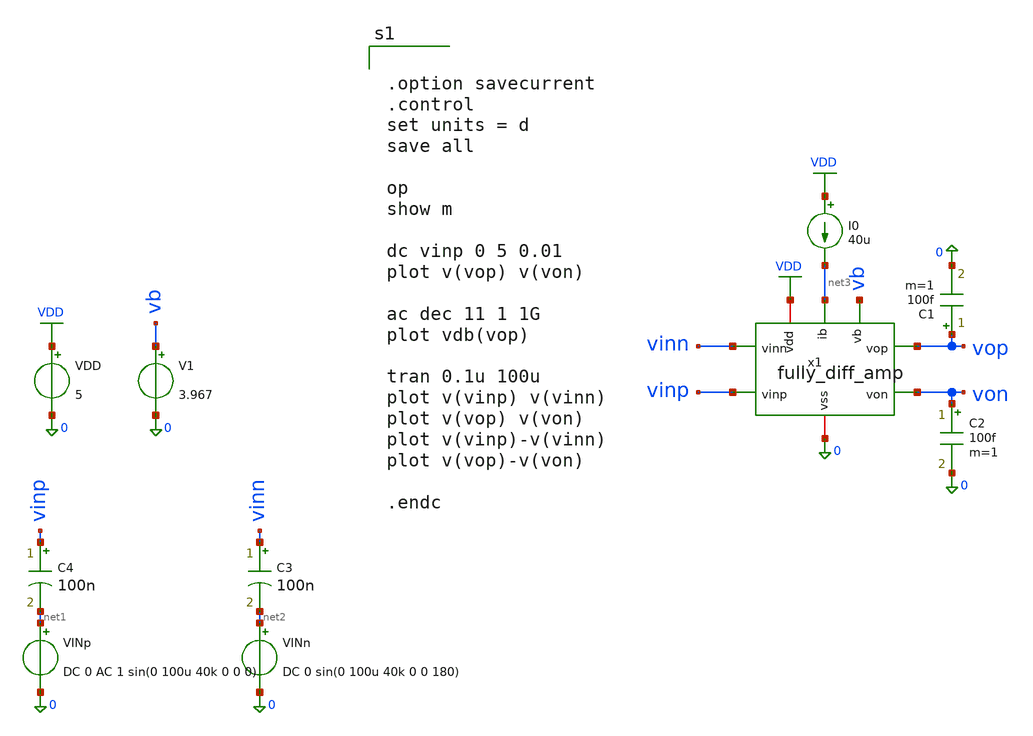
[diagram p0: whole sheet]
** sch_path: member_project/JJY_Receiver/Masahiro/jjy_recv/diff_amp/fully_diff_amp_sim.sch
**.subckt fully_diff_amp_sim
VDD VDD 0 5
VINp net1 0 DC 0 AC 1 sin(0 100u 40k 0 0 0)
V1 vb 0 3.967
VINn net2 0 DC 0 sin(0 100u 40k 0 0 180)
C3 vinn net2 100n m=1
C4 vinp net1 100n m=1
I0 VDD net3 40u
C1 vop 0 100f m=1
C2 von 0 100f m=1
x1 vb VDD vop von 0 vinn vinp net3 fully_diff_amp
**** begin user architecture code
 .include $::LIB/ip62_models


.option savecurrent
.control
set units = d
save all

op
show m

dc vinp 0 5 0.01
plot v(vop) v(von)

ac dec 11 1 1G
plot vdb(vop)

tran 0.1u 100u
plot v(vinp) v(vinn)
plot v(vop) v(von)
plot v(vinp)-v(vinn)
plot v(vop)-v(von)

.endc


**** end user architecture code
**.ends

* expanding   symbol:
*+  /home/ishi-kai/ISHI-KAI_Multiple_Projects_OpenMPW_OpenSUSI-TR10-1/member_project/JJY_Receiver/Masahiro/jjy_recv/diff_amp/fully_diff_amp.sym # of pins=8
** sym_path: member_project/JJY_Receiver/Masahiro/jjy_recv/diff_amp/fully_diff_amp.sym
** sch_path: member_project/JJY_Receiver/Masahiro/jjy_recv/diff_amp/fully_diff_amp.sch
.subckt fully_diff_amp vb vdd vop von vss vinn vinp ib
*.opin vop
*.opin von
*.ipin vinp
*.ipin vb
*.ipin ib
*.ipin vinn
*.iopin vdd
*.iopin vss
XM1 vop vb vdd vdd PMOS w=45u l=2u as=0 ad=0 ps=0 pd=0 nrd=0 nrs=0 m=1
XM2 von vb vdd vdd PMOS w=45u l=2u as=0 ad=0 ps=0 pd=0 nrd=0 nrs=0 m=1
XM3 net1 ib vss vss NMOS w=20u l=2u as=0 ad=0 ps=0 pd=0 nrd=0 nrs=0 m=1
XM4 ib ib vss vss NMOS w=20u l=2u as=0 ad=0 ps=0 pd=0 nrd=0 nrs=0 m=1
XM7 von vinp net1 vss NMOS w=20u l=2u as=0 ad=0 ps=0 pd=0 nrd=0 nrs=0 m=1
XM8 vop vinn net1 vss NMOS w=20u l=2u as=0 ad=0 ps=0 pd=0 nrd=0 nrs=0 m=1
XM6 net2 net2 vop vdd PMOS w=3.4u l=2u as=0 ad=0 ps=0 pd=0 nrd=0 nrs=0 m=1
XM9 net2 net2 vinn vdd PMOS w=3.4u l=2u as=0 ad=0 ps=0 pd=0 nrd=0 nrs=0 m=1
XM5 net3 net3 von vdd PMOS w=3.4u l=2u as=0 ad=0 ps=0 pd=0 nrd=0 nrs=0 m=1
XM10 net3 net3 vinp vdd PMOS w=3.4u l=2u as=0 ad=0 ps=0 pd=0 nrd=0 nrs=0 m=1
XM12 vinn vinn vss vss NMOS w=3.4u l=2u as=0 ad=0 ps=0 pd=0 nrd=0 nrs=0 m=1
XM13 vinn vinn vdd vdd PMOS w=8.6u l=2u as=0 ad=0 ps=0 pd=0 nrd=0 nrs=0 m=1
XM11 vinp vinp vss vss NMOS w=3.4u l=2u as=0 ad=0 ps=0 pd=0 nrd=0 nrs=0 m=1
XM14 vinp vinp vdd vdd PMOS w=8.6u l=2u as=0 ad=0 ps=0 pd=0 nrd=0 nrs=0 m=1
.ends

.GLOBAL VDD
.end
